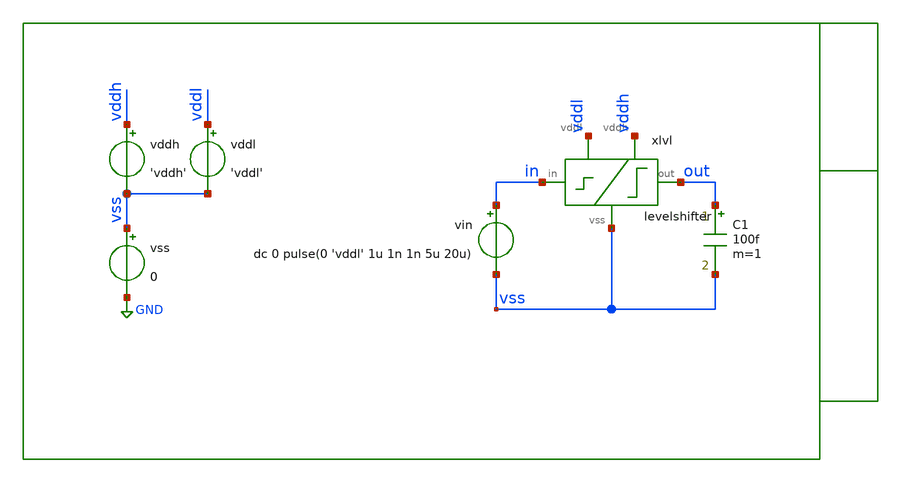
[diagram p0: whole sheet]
** sch_path: xschem/tb/levelshifter/levelshifter/tr_levelshifter.sch
**.subckt tr_levelshifter
vddh vddh vss 'vddh'
vss vss GND 0
vin in vss dc 0 pulse(0 'vddl' 1u 1n 1n 5u 20u)
C1 out vss 100f m=1
vddl vddl vss 'vddl'
xlvl vddl in out vss vddh levelshifter
**** begin user architecture code

* Control

.param vddh = 5.0
.param vddl = 3.3

.temp 27

.control
save all
tran 1n 10u uic

meas tran vsup find v(vddh) at=0.5u

let vth_hi = vsup*0.9
let vth_lo = vsup*0.1

meas tran t_lh_lo WHEN v(out)=vth_lo RISE=1
meas tran t_lh_hi WHEN v(out)=vth_hi RISE=1
meas tran t_hl_hi WHEN v(out)=vth_hi FALL=1
meas tran t_hl_lo WHEN v(out)=vth_lo FALL=1

meas tran vhi find v(out) at=2u
meas tran vlo find v(out) at=7u

let trise = t_lh_hi - t_lh_lo
let tfall = t_hl_lo - t_hl_hi

print trise
print tfall
print vhi
print vlo

.endc
.end


 * Model Corners

.include $::CORNERS/ngspice/tt.spice
*.include $::CORNERS/ngspice/ff.spice
*.include $::CORNERS/ngspice/ss.spice
*.include $::CORNERS/ngspice/sf.spice
*.include $::CORNERS/ngspice/fs.spice

**** end user architecture code
**.ends

* expanding   symbol:  sch/levelshifter/levelshifter/levelshifter.sym # of pins=5
** sym_path: xschem/sch/levelshifter/levelshifter/levelshifter.sym
** sch_path: xschem/sch/levelshifter/levelshifter/levelshifter.sch
.subckt levelshifter vddl in out vss vddh
*.iopin vddl
*.ipin in
*.opin out
*.iopin vddh
*.iopin vss
XMI1 inb_buf in vss vss nfet_06v0 L=1u W=4u nf=1 ad='int((nf+1)/2) * W/nf * 0.18u' as='int((nf+2)/2) * W/nf * 0.18u'
+ pd='2*int((nf+1)/2) * (W/nf + 0.18u)' ps='2*int((nf+2)/2) * (W/nf + 0.18u)' nrd='0.18u / W' nrs='0.18u / W'
+ sa=0 sb=0 sd=0 m=1 par=1
XMI2 in_buf inb_buf vss vss nfet_06v0 L=1u W=4u nf=1 ad='int((nf+1)/2) * W/nf * 0.18u' as='int((nf+2)/2) * W/nf * 0.18u'
+ pd='2*int((nf+1)/2) * (W/nf + 0.18u)' ps='2*int((nf+2)/2) * (W/nf + 0.18u)' nrd='0.18u / W' nrs='0.18u / W'
+ sa=0 sb=0 sd=0 m=1 par=1
XM1 outb in_buf vss vss nfet_06v0 L=1u W=8u nf=1 ad='int((nf+1)/2) * W/nf * 0.18u' as='int((nf+2)/2) * W/nf * 0.18u'
+ pd='2*int((nf+1)/2) * (W/nf + 0.18u)' ps='2*int((nf+2)/2) * (W/nf + 0.18u)' nrd='0.18u / W' nrs='0.18u / W'
+ sa=0 sb=0 sd=0 m=1 par=1
XM2 out inb_buf vss vss nfet_06v0 L=1u W=8u nf=1 ad='int((nf+1)/2) * W/nf * 0.18u' as='int((nf+2)/2) * W/nf * 0.18u'
+ pd='2*int((nf+1)/2) * (W/nf + 0.18u)' ps='2*int((nf+2)/2) * (W/nf + 0.18u)' nrd='0.18u / W' nrs='0.18u / W'
+ sa=0 sb=0 sd=0 m=1 par=1
XMI3 inb_buf in vddl vddl pfet_06v0 L=1u W=8u nf=1 ad='int((nf+1)/2) * W/nf * 0.18u' as='int((nf+2)/2) * W/nf * 0.18u'
+ pd='2*int((nf+1)/2) * (W/nf + 0.18u)' ps='2*int((nf+2)/2) * (W/nf + 0.18u)' nrd='0.18u / W' nrs='0.18u / W'
+ sa=0 sb=0 sd=0 m=1 par=1
XMI4 in_buf inb_buf vddl vddl pfet_06v0 L=1u W=8u nf=1 ad='int((nf+1)/2) * W/nf * 0.18u' as='int((nf+2)/2) * W/nf * 0.18u'
+ pd='2*int((nf+1)/2) * (W/nf + 0.18u)' ps='2*int((nf+2)/2) * (W/nf + 0.18u)' nrd='0.18u / W' nrs='0.18u / W'
+ sa=0 sb=0 sd=0 m=1 par=1
XM3 outb out vddh vddh pfet_06v0 L=1u W=2u nf=1 ad='int((nf+1)/2) * W/nf * 0.18u' as='int((nf+2)/2) * W/nf * 0.18u'
+ pd='2*int((nf+1)/2) * (W/nf + 0.18u)' ps='2*int((nf+2)/2) * (W/nf + 0.18u)' nrd='0.18u / W' nrs='0.18u / W'
+ sa=0 sb=0 sd=0 m=1 par=1
XM4 out outb vddh vddh pfet_06v0 L=1u W=2u nf=1 ad='int((nf+1)/2) * W/nf * 0.18u' as='int((nf+2)/2) * W/nf * 0.18u'
+ pd='2*int((nf+1)/2) * (W/nf + 0.18u)' ps='2*int((nf+2)/2) * (W/nf + 0.18u)' nrd='0.18u / W' nrs='0.18u / W'
+ sa=0 sb=0 sd=0 m=1 par=1
.ends

.GLOBAL GND
.end
